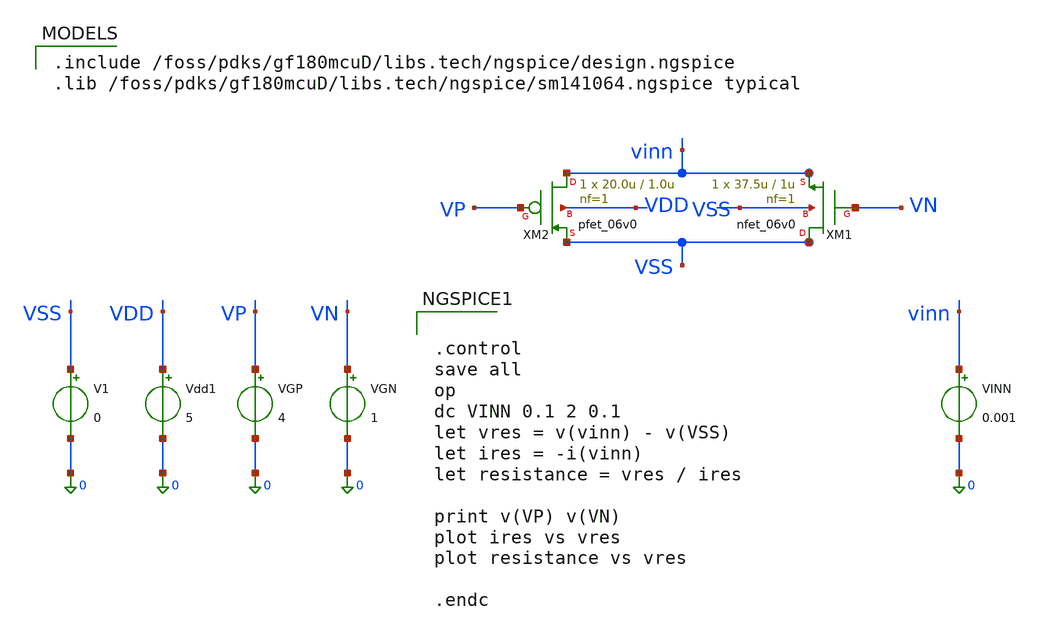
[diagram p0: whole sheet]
** sch_path: activities/opamp3An/RinLinearityCheck.sch
**.subckt RinLinearityCheck
XM1 VSS VN vinn VSS nfet_06v0 L=1u W=37.5u nf=1 ad='int((nf+1)/2) * W/nf * 0.18u' as='int((nf+2)/2) * W/nf * 0.18u'
+ pd='2*int((nf+1)/2) * (W/nf + 0.18u)' ps='2*int((nf+2)/2) * (W/nf + 0.18u)' nrd='0.18u / W' nrs='0.18u / W'
+ sa=0 sb=0 sd=0 m=1
XM2 vinn VP VSS VDD pfet_06v0 L=1.0u W=20.0u nf=1 ad='int((nf+1)/2) * W/nf * 0.18u' as='int((nf+2)/2) * W/nf * 0.18u'
+ pd='2*int((nf+1)/2) * (W/nf + 0.18u)' ps='2*int((nf+2)/2) * (W/nf + 0.18u)' nrd='0.18u / W' nrs='0.18u / W'
+ sa=0 sb=0 sd=0 m=1
V1 VSS 0 0
Vdd1 VDD 0 5
VGP VP 0 4
VGN VN 0 1
VINN vinn 0 0.001
**** begin user architecture code

.include /foss/pdks/gf180mcuD/libs.tech/ngspice/design.ngspice
.lib /foss/pdks/gf180mcuD/libs.tech/ngspice/sm141064.ngspice typical



.control
save all
op
dc VINN 0.1 2 0.1
let vres = v(vinn) - v(VSS)
let ires = -i(vinn)
let resistance = vres / ires

print v(VP) v(VN)
plot ires vs vres
plot resistance vs vres

.endc

**** end user architecture code
**.ends
.end
